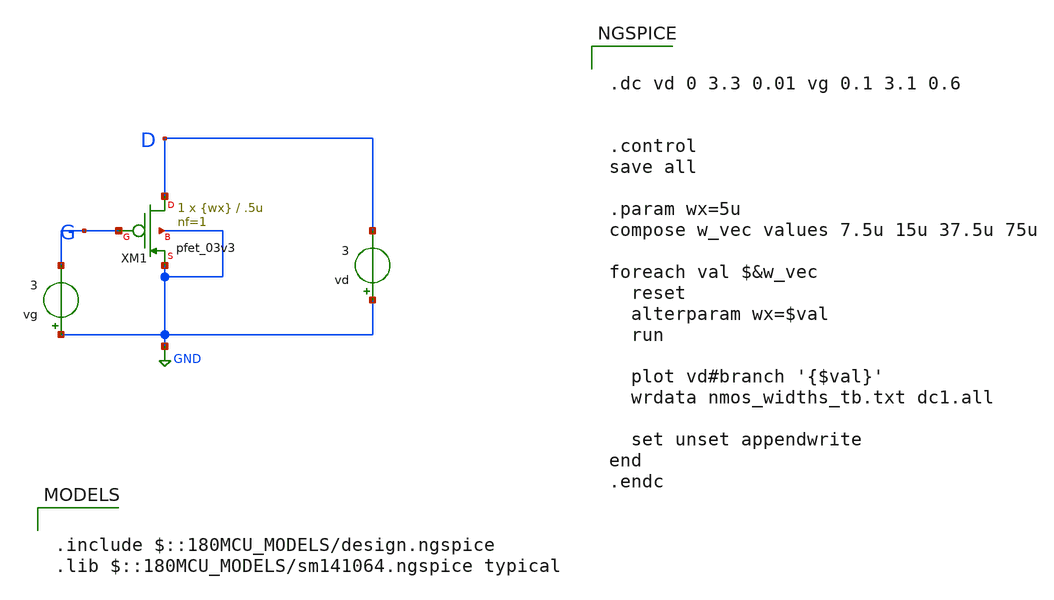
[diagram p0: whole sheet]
** sch_path: designs/libs/tb_analog/unit_transistors/pmos_widths_tb.sch
**.subckt pmos_widths_tb
vd GND D 3
vg GND G 3
XM1 D G GND GND pfet_03v3 L=.5u W={wx} nf=1 ad='int((nf+1)/2) * W/nf * 0.18u' as='int((nf+2)/2) * W/nf * 0.18u'
+ pd='2*int((nf+1)/2) * (W/nf + 0.18u)' ps='2*int((nf+2)/2) * (W/nf + 0.18u)' nrd='0.18u / W' nrs='0.18u / W'
+ sa=0 sb=0 sd=0 m=1
**** begin user architecture code

.include $::180MCU_MODELS/design.ngspice
.lib $::180MCU_MODELS/sm141064.ngspice typical



.dc vd 0 3.3 0.01 vg 0.1 3.1 0.6


.control
save all

.param wx=5u
compose w_vec values 7.5u 15u 37.5u 75u

foreach val $&w_vec
  reset
  alterparam wx=$val
  run

  plot vd#branch '{$val}'
  wrdata nmos_widths_tb.txt dc1.all

  set unset appendwrite
end
.endc


**** end user architecture code
**.ends
.GLOBAL GND
.end
